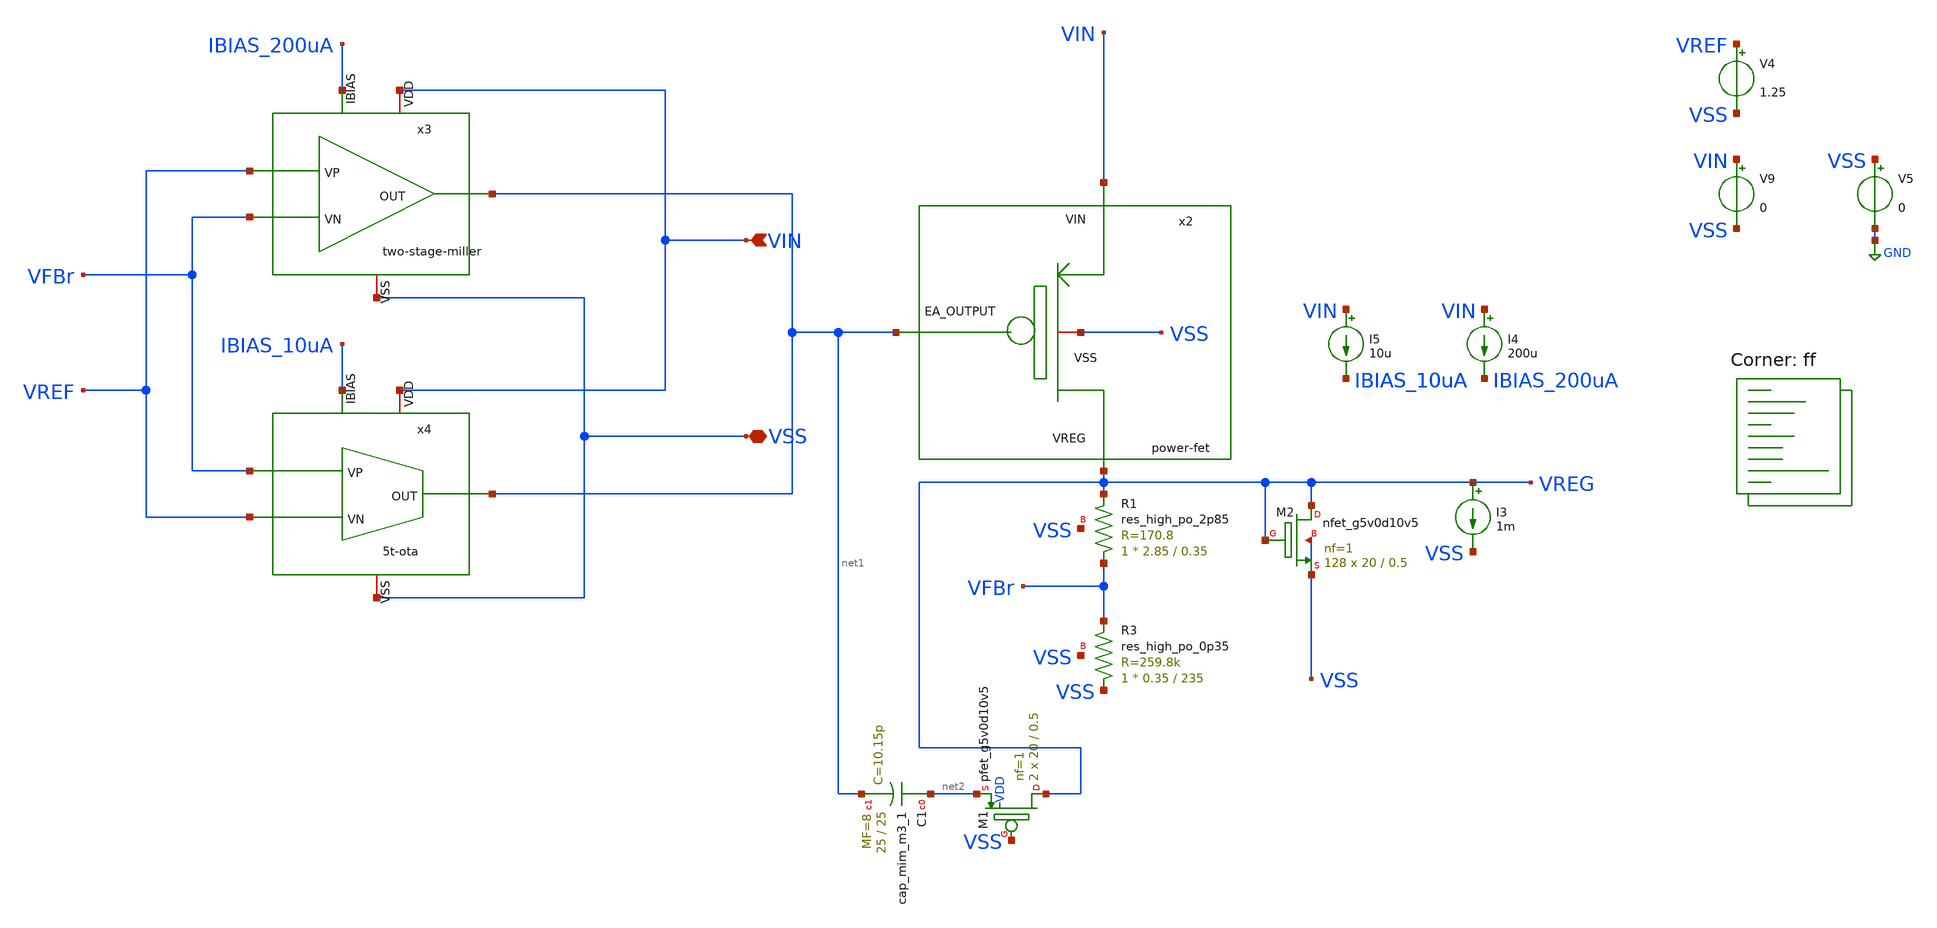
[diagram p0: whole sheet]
** sch_path: bandgap/testbench/untitled-2.sch
**.subckt untitled-2 VIN VSS
*.ipin VIN
*.iopin VSS
x2 VIN VSS net1 VREG power-fet
XR3 VSS VFBr VSS sky130_fd_pr__res_high_po_0p35 L=235 mult=1 m=1
XR1 VFBr VREG VSS sky130_fd_pr__res_high_po_2p85 L=0.35 mult=1 m=1
x3 VIN net1 VREF VFBr IBIAS_200uA VSS two-stage-miller
x4 VIN net1 IBIAS_10uA VREF VFBr VSS 5t-ota
I4 VIN IBIAS_200uA 200u
I3 VREG VSS 1m
V4 VREF VSS 1.25
V5 VSS GND 0
V9 VIN VSS 0
I5 VIN IBIAS_10uA 10u
XM2 VREG VREG VSS VSS sky130_fd_pr__nfet_g5v0d10v5 L=0.5 W=20 nf=1 ad='int((nf+1)/2) * W/nf * 0.29' as='int((nf+2)/2) * W/nf * 0.29'
+ pd='2*int((nf+1)/2) * (W/nf + 0.29)' ps='2*int((nf+2)/2) * (W/nf + 0.29)' nrd='0.29 / W' nrs='0.29 / W'
+ sa=0 sb=0 sd=0 mult=128 m=128
XC1 net2 net1 sky130_fd_pr__cap_mim_m3_1 W=25 L=25 MF=8 m=8
XM1 VREG VSS net2 VDD sky130_fd_pr__pfet_g5v0d10v5 L=0.5 W=20 nf=1 ad='int((nf+1)/2) * W/nf * 0.29' as='int((nf+2)/2) * W/nf * 0.29'
+ pd='2*int((nf+1)/2) * (W/nf + 0.29)' ps='2*int((nf+2)/2) * (W/nf + 0.29)' nrd='0.29 / W' nrs='0.29 / W'
+ sa=0 sb=0 sd=0 mult=2 m=2
**** begin user architecture code


.control
DC V9 0 5 0.01

* Nominal output voltage (from regulation region)
let Vout_nom = 1.25
let Vout_95  = 0.95*Vout_nom

* Find Vin where Vout crosses 95%
meas dc Vin_do find v(vin) when v(vreg)=Vout_95

* Measure Vout at that Vin (for completeness)
meas dc Vout_do find v(vreg) when v(vreg)=Vout_95

* Compute dropout voltage
let Vdo = Vin_do - Vout_do
print vdo
plot VIN VREG
.endc


.lib $::SKYWATER_MODELS/sky130.lib.spice ff
**** end user architecture code
**.ends
.GLOBAL GND
.end
